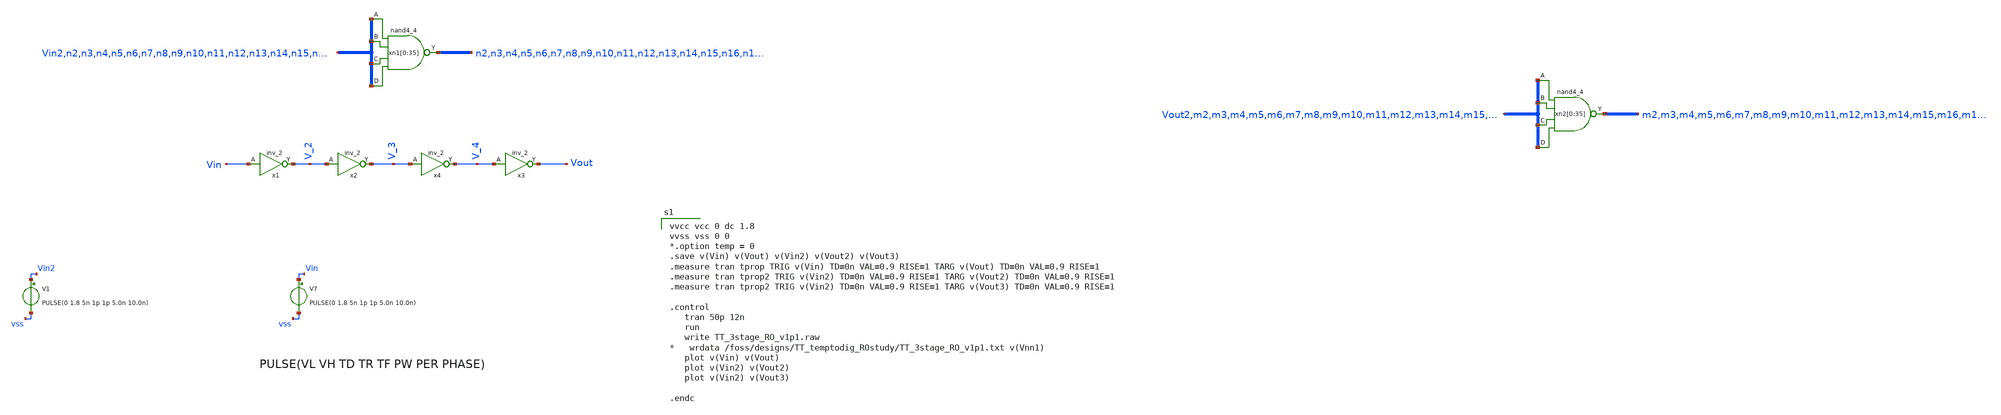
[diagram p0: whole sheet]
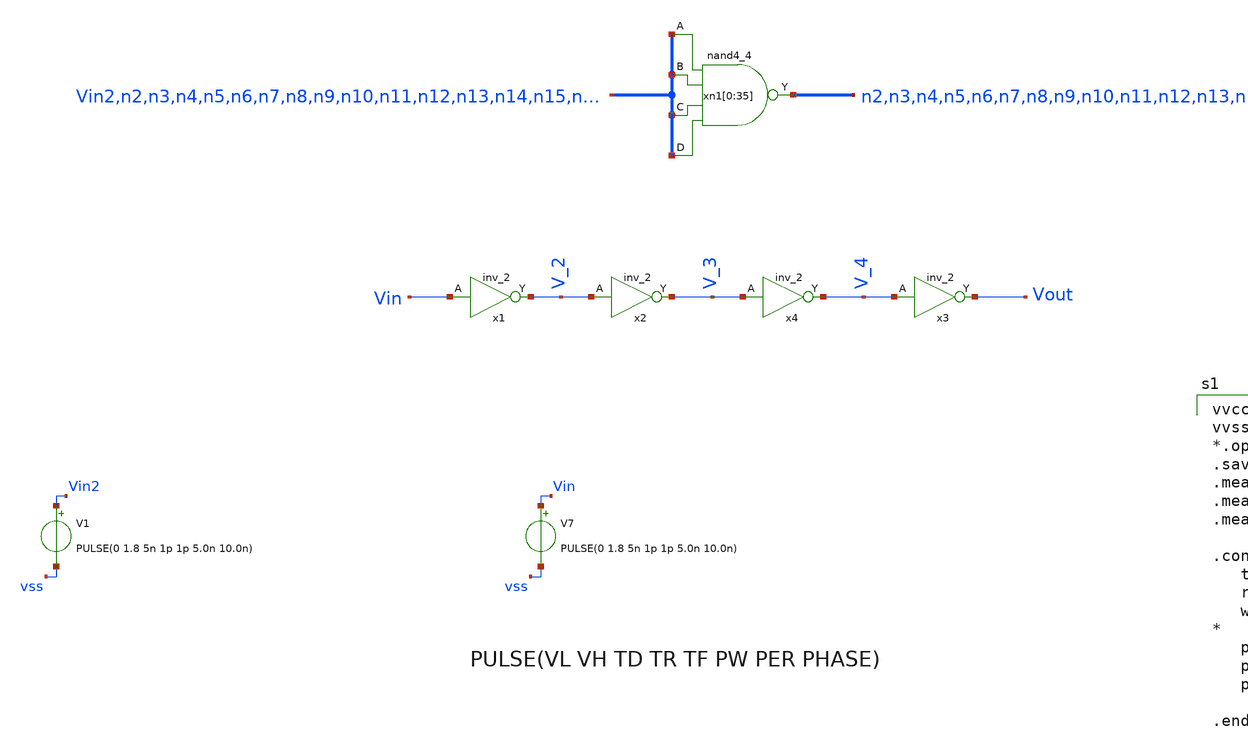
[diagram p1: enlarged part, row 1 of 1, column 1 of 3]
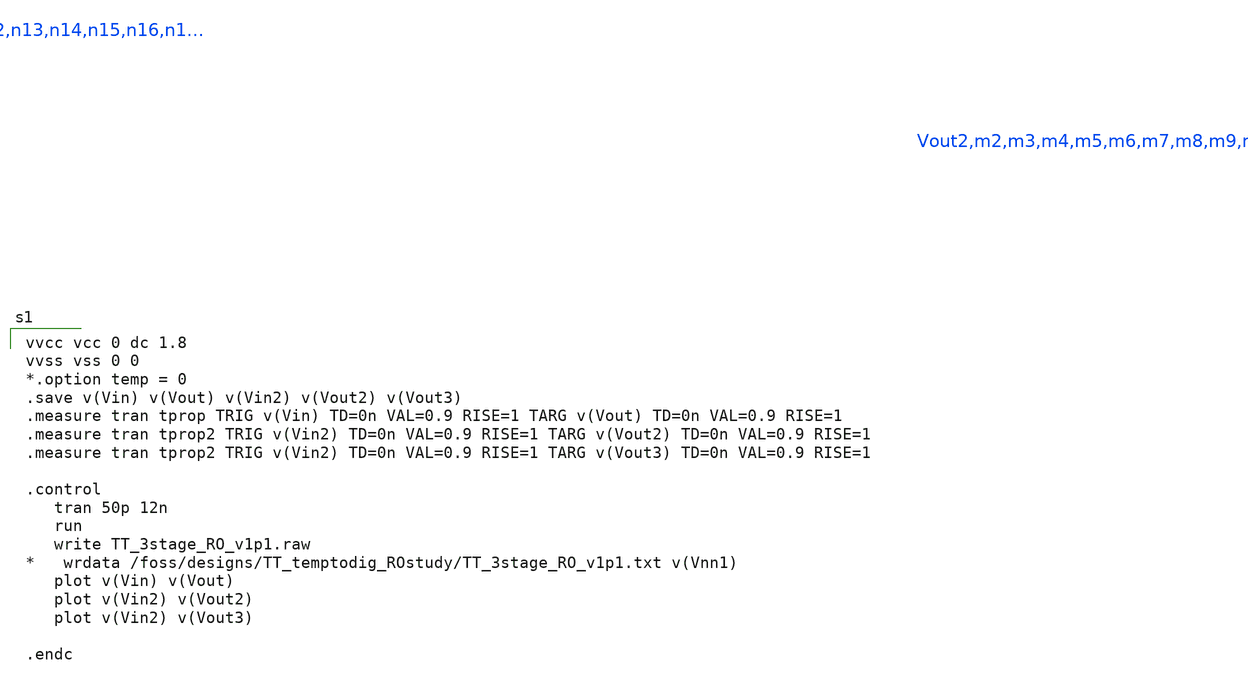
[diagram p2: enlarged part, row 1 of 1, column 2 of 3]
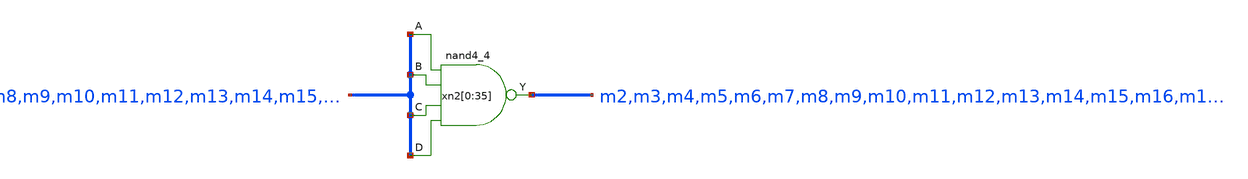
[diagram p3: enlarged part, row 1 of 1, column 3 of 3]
** sch_path: LS_boot_20230921/sch/TDC_test.sch
.lib $::SKYWATER_MODELS/sky130.lib.spice tt
.include $::SKYWATER_STDCELLS/sky130_fd_sc_hd.spice

**.subckt TDC_test
x1 Vin VSS VSS VCC VCC V_2 sky130_fd_sc_hd__inv_2
x2 V_2 VSS VSS VCC VCC V_3 sky130_fd_sc_hd__inv_2
x3 V_4 VSS VSS VCC VCC Vout sky130_fd_sc_hd__inv_2
V7 Vin vss PULSE(0 1.8 5n 1p 1p 5.0n 10.0n)
x4 V_3 VSS VSS VCC VCC V_4 sky130_fd_sc_hd__inv_2
V1 Vin2 vss PULSE(0 1.8 5n 1p 1p 5.0n 10.0n)
xn1[0] Vin2 Vin2 Vin2 Vin2 VSS VSS VCC VCC n2 sky130_fd_sc_hd__nand4_4
xn1[1] n2 n2 n2 n2 VSS VSS VCC VCC n3 sky130_fd_sc_hd__nand4_4
xn1[2] n3 n3 n3 n3 VSS VSS VCC VCC n4 sky130_fd_sc_hd__nand4_4
xn1[3] n4 n4 n4 n4 VSS VSS VCC VCC n5 sky130_fd_sc_hd__nand4_4
xn1[4] n5 n5 n5 n5 VSS VSS VCC VCC n6 sky130_fd_sc_hd__nand4_4
xn1[5] n6 n6 n6 n6 VSS VSS VCC VCC n7 sky130_fd_sc_hd__nand4_4
xn1[6] n7 n7 n7 n7 VSS VSS VCC VCC n8 sky130_fd_sc_hd__nand4_4
xn1[7] n8 n8 n8 n8 VSS VSS VCC VCC n9 sky130_fd_sc_hd__nand4_4
xn1[8] n9 n9 n9 n9 VSS VSS VCC VCC n10 sky130_fd_sc_hd__nand4_4
xn1[9] n10 n10 n10 n10 VSS VSS VCC VCC n11 sky130_fd_sc_hd__nand4_4
xn1[10] n11 n11 n11 n11 VSS VSS VCC VCC n12 sky130_fd_sc_hd__nand4_4
xn1[11] n12 n12 n12 n12 VSS VSS VCC VCC n13 sky130_fd_sc_hd__nand4_4
xn1[12] n13 n13 n13 n13 VSS VSS VCC VCC n14 sky130_fd_sc_hd__nand4_4
xn1[13] n14 n14 n14 n14 VSS VSS VCC VCC n15 sky130_fd_sc_hd__nand4_4
xn1[14] n15 n15 n15 n15 VSS VSS VCC VCC n16 sky130_fd_sc_hd__nand4_4
xn1[15] n16 n16 n16 n16 VSS VSS VCC VCC n17 sky130_fd_sc_hd__nand4_4
xn1[16] n17 n17 n17 n17 VSS VSS VCC VCC n18 sky130_fd_sc_hd__nand4_4
xn1[17] n18 n18 n18 n18 VSS VSS VCC VCC n19 sky130_fd_sc_hd__nand4_4
xn1[18] n19 n19 n19 n19 VSS VSS VCC VCC n20 sky130_fd_sc_hd__nand4_4
xn1[19] n20 n20 n20 n20 VSS VSS VCC VCC n21 sky130_fd_sc_hd__nand4_4
xn1[20] n21 n21 n21 n21 VSS VSS VCC VCC n22 sky130_fd_sc_hd__nand4_4
xn1[21] n22 n22 n22 n22 VSS VSS VCC VCC n23 sky130_fd_sc_hd__nand4_4
xn1[22] n23 n23 n23 n23 VSS VSS VCC VCC n24 sky130_fd_sc_hd__nand4_4
xn1[23] n24 n24 n24 n24 VSS VSS VCC VCC n25 sky130_fd_sc_hd__nand4_4
xn1[24] n25 n25 n25 n25 VSS VSS VCC VCC n26 sky130_fd_sc_hd__nand4_4
xn1[25] n26 n26 n26 n26 VSS VSS VCC VCC n27 sky130_fd_sc_hd__nand4_4
xn1[26] n27 n27 n27 n27 VSS VSS VCC VCC n28 sky130_fd_sc_hd__nand4_4
xn1[27] n28 n28 n28 n28 VSS VSS VCC VCC n29 sky130_fd_sc_hd__nand4_4
xn1[28] n29 n29 n29 n29 VSS VSS VCC VCC n30 sky130_fd_sc_hd__nand4_4
xn1[29] n30 n30 n30 n30 VSS VSS VCC VCC n31 sky130_fd_sc_hd__nand4_4
xn1[30] n31 n31 n31 n31 VSS VSS VCC VCC n32 sky130_fd_sc_hd__nand4_4
xn1[31] n32 n32 n32 n32 VSS VSS VCC VCC n33 sky130_fd_sc_hd__nand4_4
xn1[32] n33 n33 n33 n33 VSS VSS VCC VCC n34 sky130_fd_sc_hd__nand4_4
xn1[33] n34 n34 n34 n34 VSS VSS VCC VCC n35 sky130_fd_sc_hd__nand4_4
xn1[34] n35 n35 n35 n35 VSS VSS VCC VCC n36 sky130_fd_sc_hd__nand4_4
xn1[35] n36 n36 n36 n36 VSS VSS VCC VCC Vout2 sky130_fd_sc_hd__nand4_4
xn2[0] Vout2 Vout2 Vout2 Vout2 VSS VSS VCC VCC m2 sky130_fd_sc_hd__nand4_4
xn2[1] m2 m2 m2 m2 VSS VSS VCC VCC m3 sky130_fd_sc_hd__nand4_4
xn2[2] m3 m3 m3 m3 VSS VSS VCC VCC m4 sky130_fd_sc_hd__nand4_4
xn2[3] m4 m4 m4 m4 VSS VSS VCC VCC m5 sky130_fd_sc_hd__nand4_4
xn2[4] m5 m5 m5 m5 VSS VSS VCC VCC m6 sky130_fd_sc_hd__nand4_4
xn2[5] m6 m6 m6 m6 VSS VSS VCC VCC m7 sky130_fd_sc_hd__nand4_4
xn2[6] m7 m7 m7 m7 VSS VSS VCC VCC m8 sky130_fd_sc_hd__nand4_4
xn2[7] m8 m8 m8 m8 VSS VSS VCC VCC m9 sky130_fd_sc_hd__nand4_4
xn2[8] m9 m9 m9 m9 VSS VSS VCC VCC m10 sky130_fd_sc_hd__nand4_4
xn2[9] m10 m10 m10 m10 VSS VSS VCC VCC m11 sky130_fd_sc_hd__nand4_4
xn2[10] m11 m11 m11 m11 VSS VSS VCC VCC m12 sky130_fd_sc_hd__nand4_4
xn2[11] m12 m12 m12 m12 VSS VSS VCC VCC m13 sky130_fd_sc_hd__nand4_4
xn2[12] m13 m13 m13 m13 VSS VSS VCC VCC m14 sky130_fd_sc_hd__nand4_4
xn2[13] m14 m14 m14 m14 VSS VSS VCC VCC m15 sky130_fd_sc_hd__nand4_4
xn2[14] m15 m15 m15 m15 VSS VSS VCC VCC m16 sky130_fd_sc_hd__nand4_4
xn2[15] m16 m16 m16 m16 VSS VSS VCC VCC m17 sky130_fd_sc_hd__nand4_4
xn2[16] m17 m17 m17 m17 VSS VSS VCC VCC m18 sky130_fd_sc_hd__nand4_4
xn2[17] m18 m18 m18 m18 VSS VSS VCC VCC m19 sky130_fd_sc_hd__nand4_4
xn2[18] m19 m19 m19 m19 VSS VSS VCC VCC m20 sky130_fd_sc_hd__nand4_4
xn2[19] m20 m20 m20 m20 VSS VSS VCC VCC m21 sky130_fd_sc_hd__nand4_4
xn2[20] m21 m21 m21 m21 VSS VSS VCC VCC m22 sky130_fd_sc_hd__nand4_4
xn2[21] m22 m22 m22 m22 VSS VSS VCC VCC m23 sky130_fd_sc_hd__nand4_4
xn2[22] m23 m23 m23 m23 VSS VSS VCC VCC m24 sky130_fd_sc_hd__nand4_4
xn2[23] m24 m24 m24 m24 VSS VSS VCC VCC m25 sky130_fd_sc_hd__nand4_4
xn2[24] m25 m25 m25 m25 VSS VSS VCC VCC m26 sky130_fd_sc_hd__nand4_4
xn2[25] m26 m26 m26 m26 VSS VSS VCC VCC m27 sky130_fd_sc_hd__nand4_4
xn2[26] m27 m27 m27 m27 VSS VSS VCC VCC m28 sky130_fd_sc_hd__nand4_4
xn2[27] m28 m28 m28 m28 VSS VSS VCC VCC m29 sky130_fd_sc_hd__nand4_4
xn2[28] m29 m29 m29 m29 VSS VSS VCC VCC m30 sky130_fd_sc_hd__nand4_4
xn2[29] m30 m30 m30 m30 VSS VSS VCC VCC m31 sky130_fd_sc_hd__nand4_4
xn2[30] m31 m31 m31 m31 VSS VSS VCC VCC m32 sky130_fd_sc_hd__nand4_4
xn2[31] m32 m32 m32 m32 VSS VSS VCC VCC m33 sky130_fd_sc_hd__nand4_4
xn2[32] m33 m33 m33 m33 VSS VSS VCC VCC m34 sky130_fd_sc_hd__nand4_4
xn2[33] m34 m34 m34 m34 VSS VSS VCC VCC m35 sky130_fd_sc_hd__nand4_4
xn2[34] m35 m35 m35 m35 VSS VSS VCC VCC m36 sky130_fd_sc_hd__nand4_4
xn2[35] m36 m36 m36 m36 VSS VSS VCC VCC Vout3 sky130_fd_sc_hd__nand4_4
**** begin user architecture code

vvcc vcc 0 dc 1.8
vvss vss 0 0
*.option temp = 0
.save v(Vin) v(Vout) v(Vin2) v(Vout2) v(Vout3)
.measure tran tprop TRIG v(Vin) TD=0n VAL=0.9 RISE=1 TARG v(Vout) TD=0n VAL=0.9 RISE=1
.measure tran tprop2 TRIG v(Vin2) TD=0n VAL=0.9 RISE=1 TARG v(Vout2) TD=0n VAL=0.9 RISE=1
.measure tran tprop2 TRIG v(Vin2) TD=0n VAL=0.9 RISE=1 TARG v(Vout3) TD=0n VAL=0.9 RISE=1

.control
   tran 50p 12n
   run
   write TT_3stage_RO_v1p1.raw
*   wrdata /foss/designs/TT_temptodig_ROstudy/TT_3stage_RO_v1p1.txt v(Vnn1)
   plot v(Vin) v(Vout)
   plot v(Vin2) v(Vout2)
   plot v(Vin2) v(Vout3)

.endc


**** end user architecture code
**.ends
.end
